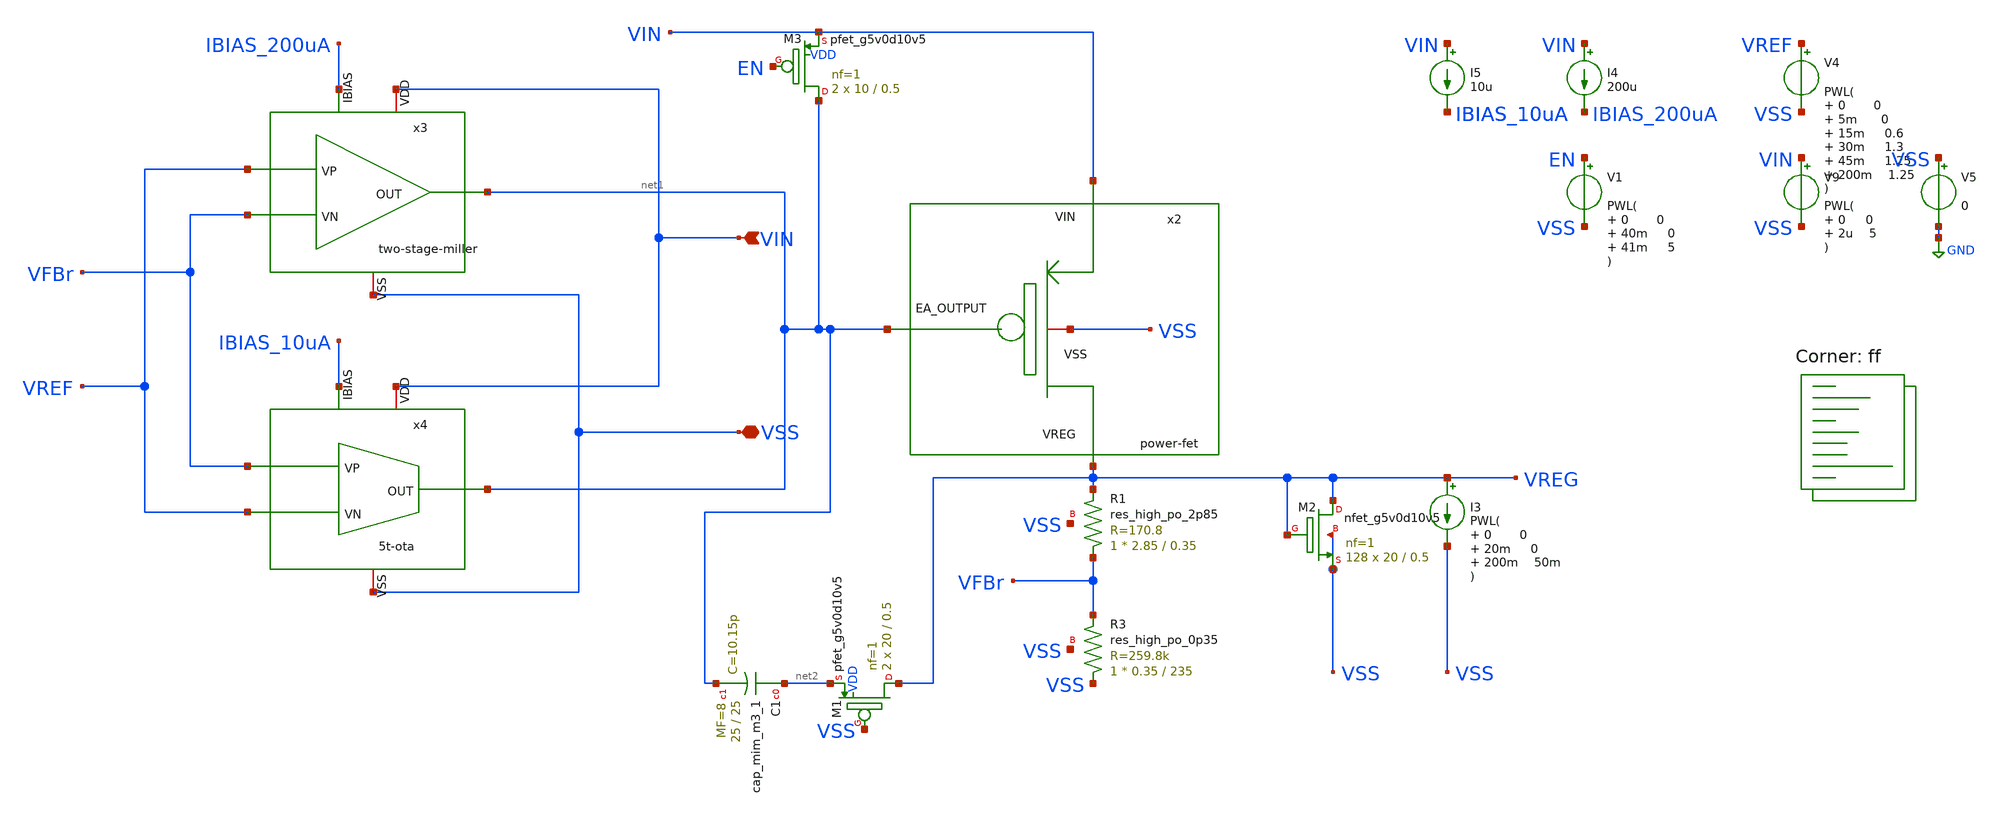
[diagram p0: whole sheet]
** sch_path: bandgap/testbench/tb_tran_startup.sch
**.subckt tb_tran_startup VIN VSS
*.ipin VIN
*.iopin VSS
x2 VIN VSS net1 VREG power-fet
XR3 VSS VFBr VSS sky130_fd_pr__res_high_po_0p35 L=235 mult=1 m=1
XR1 VFBr VREG VSS sky130_fd_pr__res_high_po_2p85 L=0.35 mult=1 m=1
x3 VIN net1 VREF VFBr IBIAS_200uA VSS two-stage-miller
x4 VIN net1 IBIAS_10uA VREF VFBr VSS 5t-ota
I4 VIN IBIAS_200uA 200u
I3 VREG VSS PWL( 0 0 20m 0 200m 50m
)
V4 VREF VSS PWL( 0 0 5m 0 15m 0.6 30m 1.3 45m 1.25 200m 1.25
)
V5 VSS GND 0
V9 VIN VSS PWL( 0 0 2u 5
)
I5 VIN IBIAS_10uA 10u
XM2 VREG VREG VSS VSS sky130_fd_pr__nfet_g5v0d10v5 L=0.5 W=20 nf=1 ad='int((nf+1)/2) * W/nf * 0.29' as='int((nf+2)/2) * W/nf * 0.29'
+ pd='2*int((nf+1)/2) * (W/nf + 0.29)' ps='2*int((nf+2)/2) * (W/nf + 0.29)' nrd='0.29 / W' nrs='0.29 / W'
+ sa=0 sb=0 sd=0 mult=128 m=128
XC1 net2 net1 sky130_fd_pr__cap_mim_m3_1 W=25 L=25 MF=8 m=8
XM1 VREG VSS net2 VDD sky130_fd_pr__pfet_g5v0d10v5 L=0.5 W=20 nf=1 ad='int((nf+1)/2) * W/nf * 0.29' as='int((nf+2)/2) * W/nf * 0.29'
+ pd='2*int((nf+1)/2) * (W/nf + 0.29)' ps='2*int((nf+2)/2) * (W/nf + 0.29)' nrd='0.29 / W' nrs='0.29 / W'
+ sa=0 sb=0 sd=0 mult=2 m=2
XM3 net1 EN VIN VDD sky130_fd_pr__pfet_g5v0d10v5 L=0.5 W=10 nf=1 ad='int((nf+1)/2) * W/nf * 0.29' as='int((nf+2)/2) * W/nf * 0.29'
+ pd='2*int((nf+1)/2) * (W/nf + 0.29)' ps='2*int((nf+2)/2) * (W/nf + 0.29)' nrd='0.29 / W' nrs='0.29 / W'
+ sa=0 sb=0 sd=0 mult=2 m=2
V1 EN VSS PWL( 0 0 40m 0 41m 5
)
**** begin user architecture code



.temp 27
.control

tran 10u 200m

* Nominal output voltage (from regulation region)
let Vout_nom = 1.25
let Vout_95  = 0.95*Vout_nom

* Find Vin where Vout crosses 95%
meas dc Vin_do find v(vin) when v(vreg)=Vout_95

* Measure Vout at that Vin (for completeness)
meas dc Vout_do find v(vreg) when v(vreg)=Vout_95

* Compute dropout voltage
let Vdo = Vin_do - Vout_do

* Compute overshoot, undershoot and peak-to-peak voltage
meas tran Vout_max MAX v(VREGloadtran)
meas tran Vout_min MIN v(VREGloadtran)
let vpp = Vout_max - Vout_min

print Vin_do Vout_do Vdo
print Vout_max Vout_min Vpp
plot VREG EN VIN VREF
plot VREGloadtran2
plot VREG
plot VIN
plot I(load)

.endc


.lib $::SKYWATER_MODELS/sky130.lib.spice ff
**** end user architecture code
**.ends
.GLOBAL GND
.end
